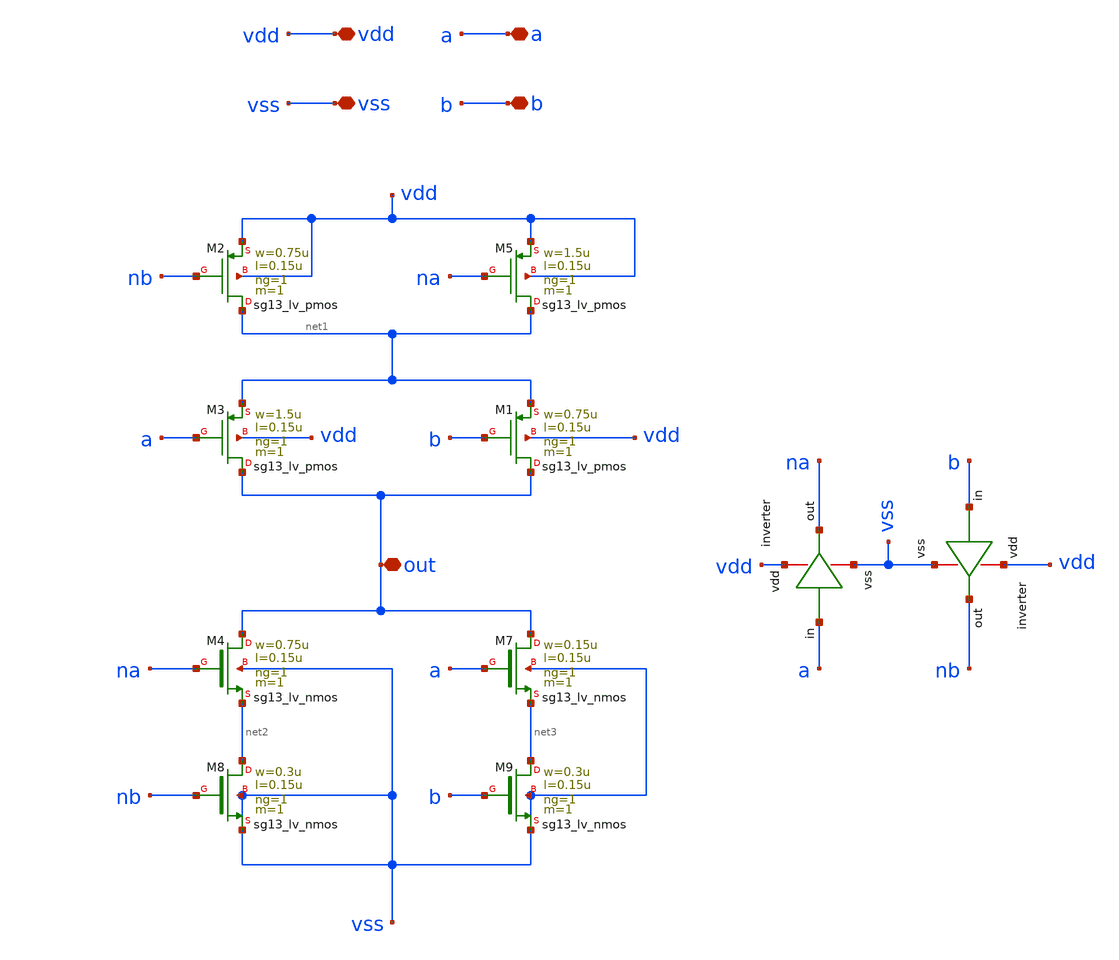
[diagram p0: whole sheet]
** sch_path: design/blocks/xorgate/schematic/xorgate.sch
**.subckt xorgate a b vdd vss out
*.iopin a
*.iopin b
*.iopin vdd
*.iopin vss
*.iopin out
XM3 out a net1 vdd sg13_lv_pmos w=1.5u l=0.15u ng=1 m=1 mm_ok=1
XM1 out b net1 vdd sg13_lv_pmos w=0.75u l=0.15u ng=1 m=1 mm_ok=1
XM4 out na net2 vss sg13_lv_nmos w=0.75u l=0.15u ng=1 m=1 mm_ok=1
x1 vdd nb b vss inverter
x2 vdd na a vss inverter
XM2 net1 nb vdd vdd sg13_lv_pmos w=0.75u l=0.15u ng=1 m=1 mm_ok=1
XM5 net1 na vdd vdd sg13_lv_pmos w=1.5u l=0.15u ng=1 m=1 mm_ok=1
XM7 out a net3 vss sg13_lv_nmos w=0.15u l=0.15u ng=1 m=1 mm_ok=1
XM8 net2 nb vss vss sg13_lv_nmos w=0.3u l=0.15u ng=1 m=1 mm_ok=1
XM9 net3 b vss vss sg13_lv_nmos w=0.3u l=0.15u ng=1 m=1 mm_ok=1
**.ends

* expanding   symbol:  blocks/inverter/schematic/inverter.sym # of pins=4
** sym_path: design/blocks/inverter/schematic/inverter.sym
** sch_path: design/blocks/inverter/schematic/inverter.sch
.subckt inverter vdd out in vss
*.iopin vdd
*.iopin out
*.iopin vss
*.iopin in
XM1 out in vss vss sky130_fd_pr__nfet_01v8 L=0.15 W=0.75 nf=1 ad='int((nf+1)/2) * W/nf * 0.29' as='int((nf+2)/2) * W/nf * 0.29'
+ pd='2*int((nf+1)/2) * (W/nf + 0.29)' ps='2*int((nf+2)/2) * (W/nf + 0.29)' nrd='0.29 / W' nrs='0.29 / W'
+ sa=0 sb=0 sd=0 mult=1 m=1
XM2 out in vdd vdd sky130_fd_pr__pfet_01v8 L=0.15 W=1.5 nf=1 ad='int((nf+1)/2) * W/nf * 0.29' as='int((nf+2)/2) * W/nf * 0.29'
+ pd='2*int((nf+1)/2) * (W/nf + 0.29)' ps='2*int((nf+2)/2) * (W/nf + 0.29)' nrd='0.29 / W' nrs='0.29 / W'
+ sa=0 sb=0 sd=0 mult=1 m=1
.ends

.end
